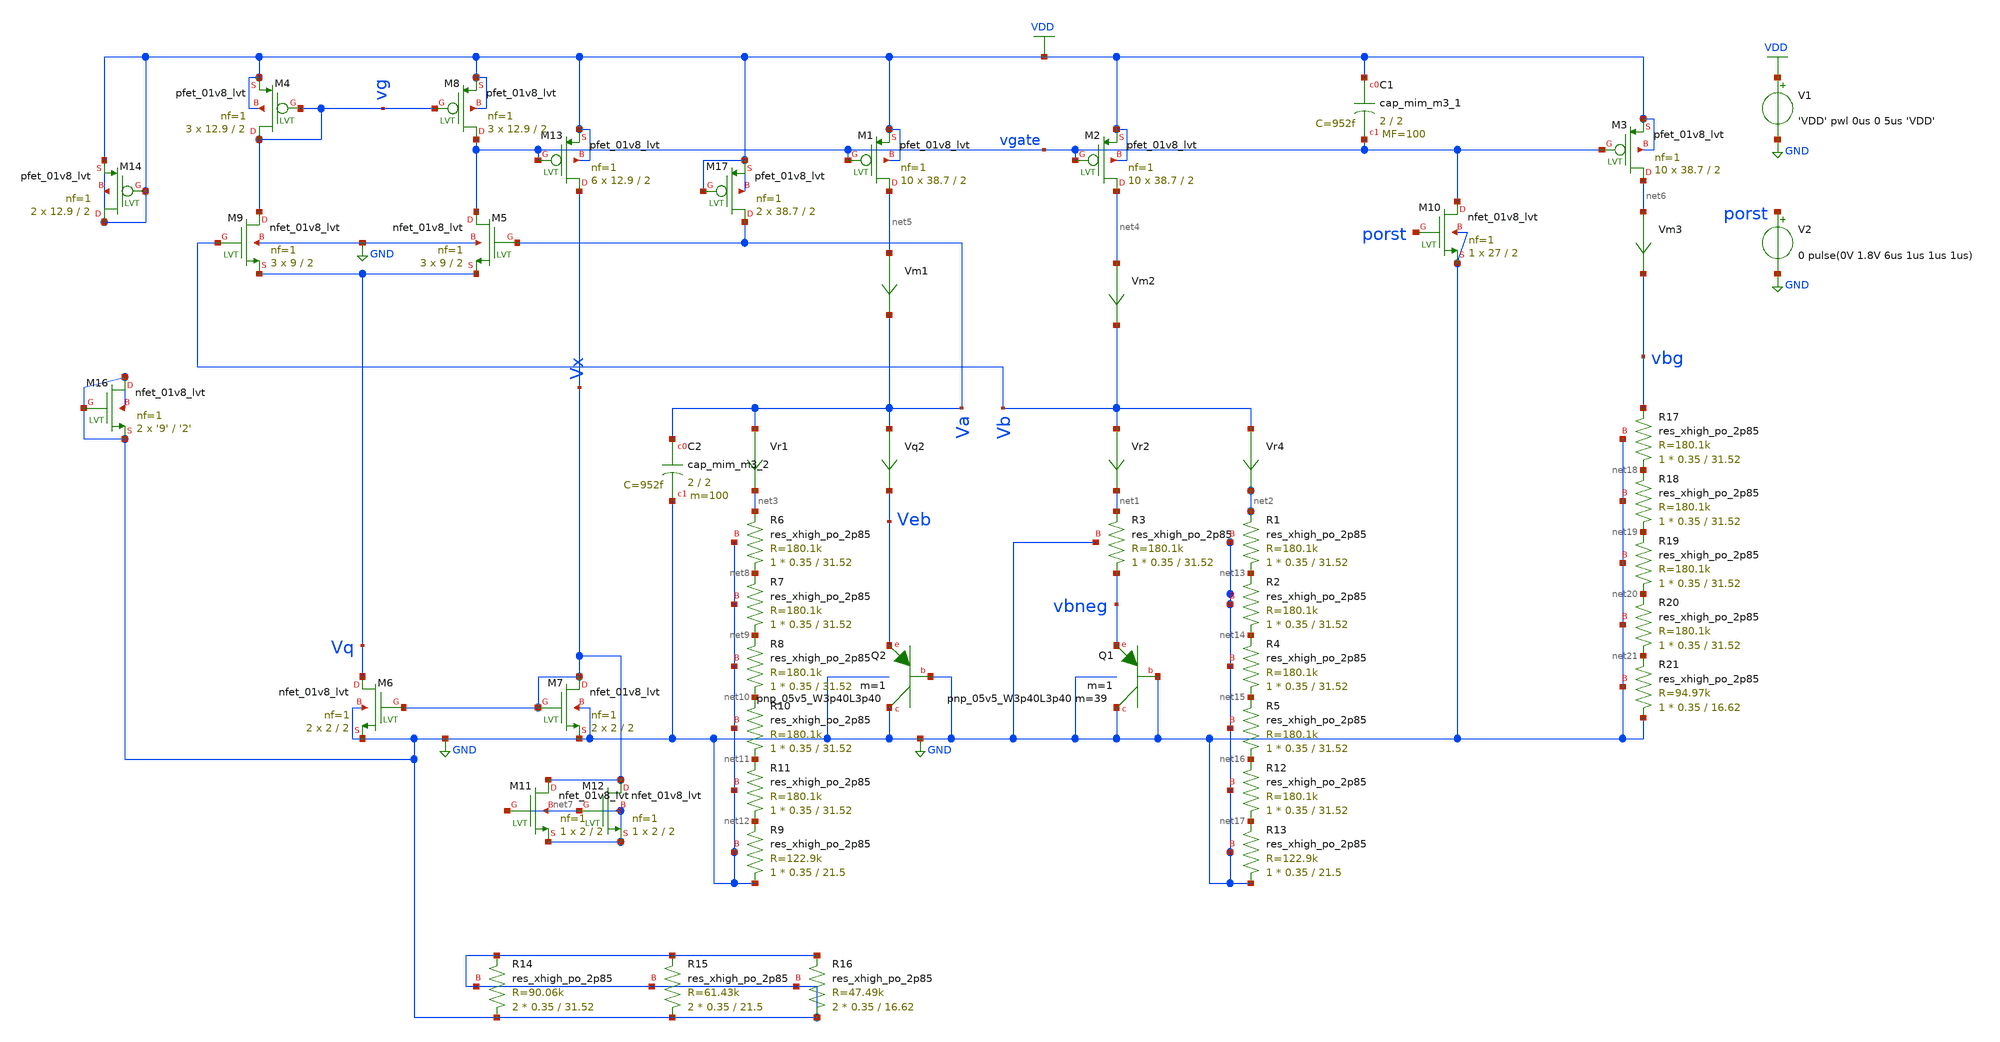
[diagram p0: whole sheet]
** sch_path: tests/dc_op/tsmc_bandgap_real_op_layout.sch
**.subckt tsmc_bandgap_real_op_layout
V1 VDD GND 'VDD' pwl 0us 0 5us 'VDD'
XQ2 GND GND Veb sky130_fd_pr__pnp_05v5_W3p40L3p40 m=1
Vr4 Vb net2 0
.save i(vr4)
Vr2 Vb net1 0
.save i(vr2)
Vm1 net5 Va 0
.save i(vm1)
Vm2 net4 Vb 0
.save i(vm2)
Vm3 net6 vbg 0
.save i(vm3)
Vr1 Va net3 0
.save i(vr1)
Vq2 Va Veb 0
.save i(vq2)
XQ1 GND GND vbneg sky130_fd_pr__pnp_05v5_W3p40L3p40 m=39 m=1
XM5 vgate Va Vq GND sky130_fd_pr__nfet_01v8_lvt L=2 W=9 nf=1 ad='int((nf+1)/2) * W/nf * 0.29' as='int((nf+2)/2) * W/nf * 0.29'
+ pd='2*int((nf+1)/2) * (W/nf + 0.29)' ps='2*int((nf+2)/2) * (W/nf + 0.29)' nrd='0.29 / W' nrs='0.29 / W'
+ sa=0 sb=0 sd=0 mult=3 m=3
XM6 Vq Vx GND GND sky130_fd_pr__nfet_01v8_lvt L=2 W=2 nf=1 ad='int((nf+1)/2) * W/nf * 0.29' as='int((nf+2)/2) * W/nf * 0.29'
+ pd='2*int((nf+1)/2) * (W/nf + 0.29)' ps='2*int((nf+2)/2) * (W/nf + 0.29)' nrd='0.29 / W' nrs='0.29 / W'
+ sa=0 sb=0 sd=0 mult=2 m=2
XM9 vg Vb Vq GND sky130_fd_pr__nfet_01v8_lvt L=2 W=9 nf=1 ad='int((nf+1)/2) * W/nf * 0.29' as='int((nf+2)/2) * W/nf * 0.29'
+ pd='2*int((nf+1)/2) * (W/nf + 0.29)' ps='2*int((nf+2)/2) * (W/nf + 0.29)' nrd='0.29 / W' nrs='0.29 / W'
+ sa=0 sb=0 sd=0 mult=3 m=3
XM7 Vx Vx GND GND sky130_fd_pr__nfet_01v8_lvt L=2 W=2 nf=1 ad='int((nf+1)/2) * W/nf * 0.29' as='int((nf+2)/2) * W/nf * 0.29'
+ pd='2*int((nf+1)/2) * (W/nf + 0.29)' ps='2*int((nf+2)/2) * (W/nf + 0.29)' nrd='0.29 / W' nrs='0.29 / W'
+ sa=0 sb=0 sd=0 mult=2 m=2
XM13 Vx vgate VDD VDD sky130_fd_pr__pfet_01v8_lvt L=2 W=12.9 nf=1 ad='int((nf+1)/2) * W/nf * 0.29' as='int((nf+2)/2) * W/nf * 0.29'
+ pd='2*int((nf+1)/2) * (W/nf + 0.29)' ps='2*int((nf+2)/2) * (W/nf + 0.29)' nrd='0.29 / W' nrs='0.29 / W'
+ sa=0 sb=0 sd=0 mult=6 m=6
XM1 net5 vgate VDD VDD sky130_fd_pr__pfet_01v8_lvt L=2 W=38.7 nf=1 ad='int((nf+1)/2) * W/nf * 0.29' as='int((nf+2)/2) * W/nf * 0.29'
+ pd='2*int((nf+1)/2) * (W/nf + 0.29)' ps='2*int((nf+2)/2) * (W/nf + 0.29)' nrd='0.29 / W' nrs='0.29 / W'
+ sa=0 sb=0 sd=0 mult=10 m=10
XM2 net4 vgate VDD VDD sky130_fd_pr__pfet_01v8_lvt L=2 W=38.7 nf=1 ad='int((nf+1)/2) * W/nf * 0.29' as='int((nf+2)/2) * W/nf * 0.29'
+ pd='2*int((nf+1)/2) * (W/nf + 0.29)' ps='2*int((nf+2)/2) * (W/nf + 0.29)' nrd='0.29 / W' nrs='0.29 / W'
+ sa=0 sb=0 sd=0 mult=10 m=10
XM3 net6 vgate VDD VDD sky130_fd_pr__pfet_01v8_lvt L=2 W=38.7 nf=1 ad='int((nf+1)/2) * W/nf * 0.29' as='int((nf+2)/2) * W/nf * 0.29'
+ pd='2*int((nf+1)/2) * (W/nf + 0.29)' ps='2*int((nf+2)/2) * (W/nf + 0.29)' nrd='0.29 / W' nrs='0.29 / W'
+ sa=0 sb=0 sd=0 mult=10 m=10
XM4 vg vg VDD VDD sky130_fd_pr__pfet_01v8_lvt L=2 W=12.9 nf=1 ad='int((nf+1)/2) * W/nf * 0.29' as='int((nf+2)/2) * W/nf * 0.29'
+ pd='2*int((nf+1)/2) * (W/nf + 0.29)' ps='2*int((nf+2)/2) * (W/nf + 0.29)' nrd='0.29 / W' nrs='0.29 / W'
+ sa=0 sb=0 sd=0 mult=3 m=3
XM8 vgate vg VDD VDD sky130_fd_pr__pfet_01v8_lvt L=2 W=12.9 nf=1 ad='int((nf+1)/2) * W/nf * 0.29' as='int((nf+2)/2) * W/nf * 0.29'
+ pd='2*int((nf+1)/2) * (W/nf + 0.29)' ps='2*int((nf+2)/2) * (W/nf + 0.29)' nrd='0.29 / W' nrs='0.29 / W'
+ sa=0 sb=0 sd=0 mult=3 m=3
XM10 vgate porst GND GND sky130_fd_pr__nfet_01v8_lvt L=2 W=27 nf=1 ad='int((nf+1)/2) * W/nf * 0.29' as='int((nf+2)/2) * W/nf * 0.29'
+ pd='2*int((nf+1)/2) * (W/nf + 0.29)' ps='2*int((nf+2)/2) * (W/nf + 0.29)' nrd='0.29 / W' nrs='0.29 / W'
+ sa=0 sb=0 sd=0 mult=1 m=1
V2 porst GND 0 pulse(0V 1.8V 6us 1us 1us 1us)
XR6 net8 net3 GND sky130_fd_pr__res_xhigh_po_2p85 L=31.52 mult=1 m=1
XR7 net9 net8 GND sky130_fd_pr__res_xhigh_po_2p85 L=31.52 mult=1 m=1
XR8 net10 net9 GND sky130_fd_pr__res_xhigh_po_2p85 L=31.52 mult=1 m=1
XR10 net11 net10 GND sky130_fd_pr__res_xhigh_po_2p85 L=31.52 mult=1 m=1
XR11 net12 net11 GND sky130_fd_pr__res_xhigh_po_2p85 L=31.52 mult=1 m=1
XR9 GND net12 GND sky130_fd_pr__res_xhigh_po_2p85 L=21.5 mult=1 m=1
XR3 vbneg net1 GND sky130_fd_pr__res_xhigh_po_2p85 L=31.52 mult=1 m=1
XR1 net13 net2 GND sky130_fd_pr__res_xhigh_po_2p85 L=31.52 mult=1 m=1
XR2 net14 net13 GND sky130_fd_pr__res_xhigh_po_2p85 L=31.52 mult=1 m=1
XR4 net15 net14 GND sky130_fd_pr__res_xhigh_po_2p85 L=31.52 mult=1 m=1
XR5 net16 net15 GND sky130_fd_pr__res_xhigh_po_2p85 L=31.52 mult=1 m=1
XR12 net17 net16 GND sky130_fd_pr__res_xhigh_po_2p85 L=31.52 mult=1 m=1
XR13 GND net17 GND sky130_fd_pr__res_xhigh_po_2p85 L=21.5 mult=1 m=1
XR17 net18 vbg GND sky130_fd_pr__res_xhigh_po_2p85 L=31.52 mult=1 m=1
XR18 net19 net18 GND sky130_fd_pr__res_xhigh_po_2p85 L=31.52 mult=1 m=1
XR19 net20 net19 GND sky130_fd_pr__res_xhigh_po_2p85 L=31.52 mult=1 m=1
XR20 net21 net20 GND sky130_fd_pr__res_xhigh_po_2p85 L=31.52 mult=1 m=1
XR21 GND net21 GND sky130_fd_pr__res_xhigh_po_2p85 L=16.62 mult=1 m=1
XC1 VDD vgate sky130_fd_pr__cap_mim_m3_1 W=2 L=2 MF=100 m=100
XC2 Va GND sky130_fd_pr__cap_mim_m3_2 W=2 L=2 MF=100 m=100
XR14 GND GND GND sky130_fd_pr__res_xhigh_po_2p85 L=31.52 mult=2 m=2
XR15 GND GND GND sky130_fd_pr__res_xhigh_po_2p85 L=21.5 mult=2 m=2
XR16 GND GND GND sky130_fd_pr__res_xhigh_po_2p85 L=16.62 mult=2 m=2
XM11 Vx net7 net7 net7 sky130_fd_pr__nfet_01v8_lvt L=2 W=2 nf=1 ad='int((nf+1)/2) * W/nf * 0.29' as='int((nf+2)/2) * W/nf * 0.29'
+ pd='2*int((nf+1)/2) * (W/nf + 0.29)' ps='2*int((nf+2)/2) * (W/nf + 0.29)' nrd='0.29 / W' nrs='0.29 / W'
+ sa=0 sb=0 sd=0 mult=1 m=1
XM12 Vx net7 net7 net7 sky130_fd_pr__nfet_01v8_lvt L=2 W=2 nf=1 ad='int((nf+1)/2) * W/nf * 0.29' as='int((nf+2)/2) * W/nf * 0.29'
+ pd='2*int((nf+1)/2) * (W/nf + 0.29)' ps='2*int((nf+2)/2) * (W/nf + 0.29)' nrd='0.29 / W' nrs='0.29 / W'
+ sa=0 sb=0 sd=0 mult=1 m=1
XM14 VDD VDD VDD VDD sky130_fd_pr__pfet_01v8_lvt L=2 W=12.9 nf=1 ad='int((nf+1)/2) * W/nf * 0.29' as='int((nf+2)/2) * W/nf * 0.29'
+ pd='2*int((nf+1)/2) * (W/nf + 0.29)' ps='2*int((nf+2)/2) * (W/nf + 0.29)' nrd='0.29 / W' nrs='0.29 / W'
+ sa=0 sb=0 sd=0 mult=2 m=2
XM16 GND GND GND GND sky130_fd_pr__nfet_01v8_lvt L='2' W='9' nf=1 ad='int((nf+1)/2) * W/nf * 0.29' as='int((nf+2)/2) * W/nf * 0.29'
+ pd='2*int((nf+1)/2) * (W/nf + 0.29)' ps='2*int((nf+2)/2) * (W/nf + 0.29)' nrd='0.29 / W' nrs='0.29 / W'
+ sa=0 sb=0 sd=0 mult=2 m=2
XM17 Va VDD VDD VDD sky130_fd_pr__pfet_01v8_lvt L=2 W=38.7 nf=1 ad='int((nf+1)/2) * W/nf * 0.29' as='int((nf+2)/2) * W/nf * 0.29'
+ pd='2*int((nf+1)/2) * (W/nf + 0.29)' ps='2*int((nf+2)/2) * (W/nf + 0.29)' nrd='0.29 / W' nrs='0.29 / W'
+ sa=0 sb=0 sd=0 mult=2 m=2
**** begin user architecture code


.option savecurrents
.param mc_mm_switch=0
.param R3val='22.187k'
.param alpha='1'
.param R2R3ratio='5.6555038*alpha'
.param R2val='R3val*R2R3ratio'
.param R4R2ratio='0.79694273'
.param R4val='R2val*R4R2ratio
.param VDD=1.8
.nodeset v(vgate)=1.31

.control
save all  @m.xm1.msky130_fd_pr__pfet_01v8_lvt[gm]  @m.xm2.msky130_fd_pr__pfet_01v8_lvt[gm]  @m.xm3.msky130_fd_pr__pfet_01v8_lvt[gm]  @m.xm4.msky130_fd_pr__pfet_01v8_lvt[gm]  @m.xm5.msky130_fd_pr__nfet_01v8_lvt[gm]  @m.xm6.msky130_fd_pr__nfet_01v8_lvt[gm]  @m.xm7.msky130_fd_pr__nfet_01v8_lvt[gm]  @m.xm8.msky130_fd_pr__pfet_01v8_lvt[gm]  @m.xm9.msky130_fd_pr__nfet_01v8_lvt[gm]  @m.xm13.msky130_fd_pr__pfet_01v8_lvt[gm]

op
write tsmc_bandgap_real_op_layout.raw
let id8=@m.xm8.msky130_fd_pr__pfet_01v8_lvt[id]
let id1=@m.xm1.msky130_fd_pr__pfet_01v8_lvt[id]
let vth5=@m.xm5.msky130_fd_pr__nfet_01v8_lvt[vth]
let vth6=@m.xm6.msky130_fd_pr__nfet_01v8_lvt[vth]
let wm8=@m.xm8.msky130_fd_pr__pfet_01v8_lvt[w]
let mm8=@m.xm8.msky130_fd_pr__pfet_01v8_lvt[m]
let weff8=wm8*mm8
let jd8=id8/weff8
let wm1=@m.xm1.msky130_fd_pr__pfet_01v8_lvt[w]
let mm1=@m.xm1.msky130_fd_pr__pfet_01v8_lvt[m]
let weff1=wm1*mm1
let jd1=id1/weff1
let wm13=@m.xm13.msky130_fd_pr__pfet_01v8_lvt[w]
let mm13=@m.xm13.msky130_fd_pr__pfet_01v8_lvt[m]
let weff13=wm13*mm13
let id13=@m.xm13.msky130_fd_pr__pfet_01v8_lvt[id]
let jd13=id13/weff13
let gm13=@m.xm13.msky130_fd_pr__pfet_01v8_lvt[gm]
let gm3=@m.xm3.msky130_fd_pr__pfet_01v8_lvt[gm]
let gm4=@m.xm4.msky130_fd_pr__pfet_01v8_lvt[gm]
let gm5=@m.xm5.msky130_fd_pr__nfet_01v8_lvt[gm]
let gm6=@m.xm6.msky130_fd_pr__nfet_01v8_lvt[gm]
let gm7=@m.xm7.msky130_fd_pr__nfet_01v8_lvt[gm]
let gm8=@m.xm8.msky130_fd_pr__pfet_01v8_lvt[gm]
let gm9=@m.xm9.msky130_fd_pr__nfet_01v8_lvt[gm]
let gm1=@m.xm1.msky130_fd_pr__pfet_01v8_lvt[gm]
let gm2=@m.xm2.msky130_fd_pr__pfet_01v8_lvt[gm]
let vdsat1=2/(gm1/vm1#branch)
let vdsat2=2/(gm2/vm2#branch)
let vdsat3=2/(gm3/vm3#branch)
let vdsat4=2/(gm4/@m.xm4.msky130_fd_pr__pfet_01v8_lvt[id])
let vdsat5=2/(gm5/@m.xm5.msky130_fd_pr__nfet_01v8_lvt[id])
let vdsat6=2/(gm6/@m.xm6.msky130_fd_pr__nfet_01v8_lvt[id])
let vdsat7=2/(gm7/@m.xm7.msky130_fd_pr__nfet_01v8_lvt[id])
let vdsat8=2/(gm8/@m.xm8.msky130_fd_pr__pfet_01v8_lvt[id])
let vdsat9=2/(gm9/@m.xm9.msky130_fd_pr__nfet_01v8_lvt[id])
let vdsat13=2/(gm13/@m.xm13.msky130_fd_pr__pfet_01v8_lvt[id])


print vbg vgate vg va vb vx vq
print vdsat1 vdsat2 vdsat3 vdsat4   vdsat5 vdsat6 vdsat7 vdsat8 vdsat9 vdsat13
.endc



** opencircuitdesign pdks install
.lib $::SKYWATER_MODELS/sky130.lib.spice tt


**** end user architecture code
**.ends
.GLOBAL VDD
.GLOBAL GND
.end
